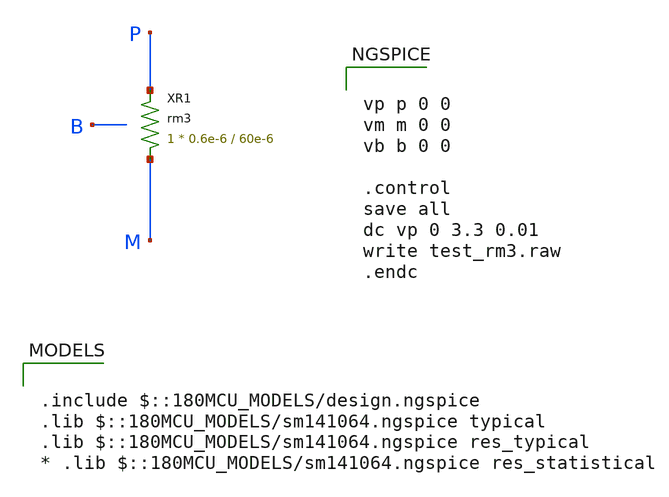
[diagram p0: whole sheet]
** sch_path: gf180mcuD/xschem_libs/gf180mcu_tests/test_rm3/schematic/test_rm3.sch
* Copyright 2022 GlobalFoundries PDK Authors
* Licensed under the Apache License, Version 2.0 (the "License");
* you may not use this file except in compliance with the License.
* You may obtain a copy of the License at
* https://www.apache.org/licenses/LICENSE-2.0
* Unless required by applicable law or agreed to in writing, software
* distributed under the License is distributed on an "AS IS" BASIS,
* WITHOUT WARRANTIES OR CONDITIONS OF ANY KIND, either express or implied.
* See the License for the specific language governing permissions and
* limitations under the License.
**.subckt test_rm3
XR1 M P rm3 r_width=0.6e-6 r_length=60e-6 m=1
**** begin user architecture code

.include $::180MCU_MODELS/design.ngspice
.lib $::180MCU_MODELS/sm141064.ngspice typical
.lib $::180MCU_MODELS/sm141064.ngspice res_typical
* .lib $::180MCU_MODELS/sm141064.ngspice res_statistical



vp p 0 0
vm m 0 0
vb b 0 0

.control
save all
dc vp 0 3.3 0.01
write test_rm3.raw
.endc


**** end user architecture code
**.ends
.end
